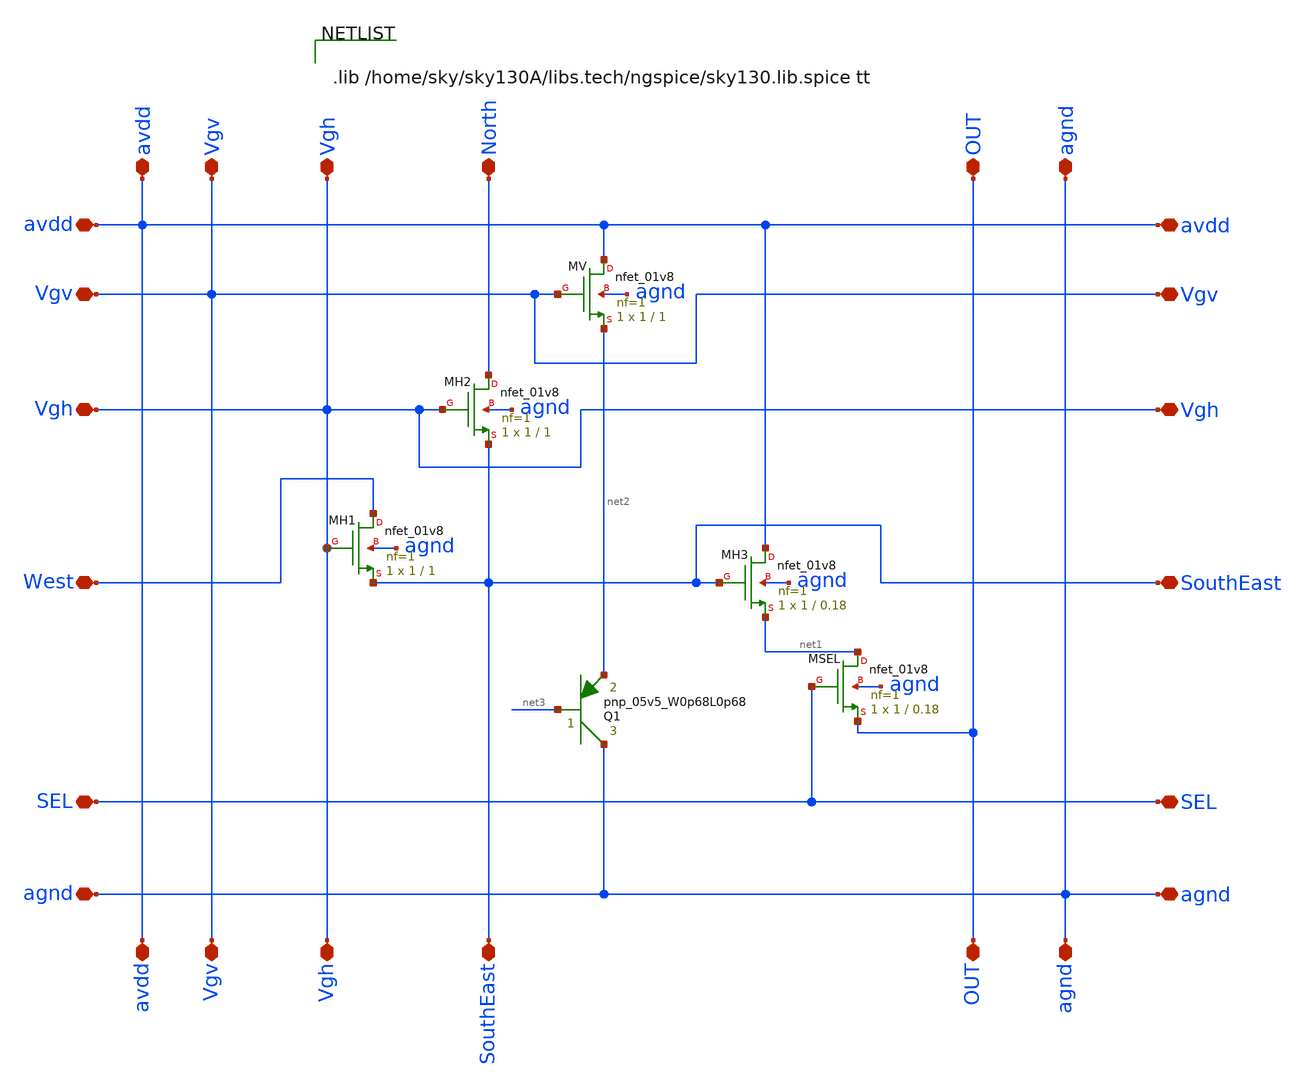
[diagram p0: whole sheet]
** sch_path: xschem/HW4_RAM_readout/pixel.sch
**.subckt pixel North SouthEast West SouthEast avdd avdd avdd avdd Vgv Vgh Vgv Vgv Vgv Vgh Vgh Vgh
*+ SEL SEL OUT OUT agnd agnd agnd agnd
*.iopin North
*.iopin SouthEast
*.iopin West
*.iopin SouthEast
*.iopin avdd
*.iopin avdd
*.iopin avdd
*.iopin avdd
*.iopin Vgv
*.iopin Vgh
*.iopin Vgv
*.iopin Vgv
*.iopin Vgv
*.iopin Vgh
*.iopin Vgh
*.iopin Vgh
*.iopin SEL
*.iopin SEL
*.iopin OUT
*.iopin OUT
*.iopin agnd
*.iopin agnd
*.iopin agnd
*.iopin agnd
XMV avdd Vgv net2 agnd sky130_fd_pr__nfet_01v8 L=1 W=1 nf=1 ad='int((nf+1)/2) * W/nf * 0.29' as='int((nf+2)/2) * W/nf * 0.29'
+ pd='2*int((nf+1)/2) * (W/nf + 0.29)' ps='2*int((nf+2)/2) * (W/nf + 0.29)' nrd='0.29 / W' nrs='0.29 / W'
+ sa=0 sb=0 sd=0 mult=1 m=1
XMH2 North Vgh SouthEast agnd sky130_fd_pr__nfet_01v8 L=1 W=1 nf=1 ad='int((nf+1)/2) * W/nf * 0.29' as='int((nf+2)/2) * W/nf * 0.29'
+ pd='2*int((nf+1)/2) * (W/nf + 0.29)' ps='2*int((nf+2)/2) * (W/nf + 0.29)' nrd='0.29 / W' nrs='0.29 / W'
+ sa=0 sb=0 sd=0 mult=1 m=1
XMH1 West Vgh SouthEast agnd sky130_fd_pr__nfet_01v8 L=1 W=1 nf=1 ad='int((nf+1)/2) * W/nf * 0.29' as='int((nf+2)/2) * W/nf * 0.29'
+ pd='2*int((nf+1)/2) * (W/nf + 0.29)' ps='2*int((nf+2)/2) * (W/nf + 0.29)' nrd='0.29 / W' nrs='0.29 / W'
+ sa=0 sb=0 sd=0 mult=1 m=1
XMH3 avdd SouthEast net1 agnd sky130_fd_pr__nfet_01v8 L=0.18 W=1 nf=1 ad='int((nf+1)/2) * W/nf * 0.29'
+ as='int((nf+2)/2) * W/nf * 0.29' pd='2*int((nf+1)/2) * (W/nf + 0.29)' ps='2*int((nf+2)/2) * (W/nf + 0.29)'
+ nrd='0.29 / W' nrs='0.29 / W' sa=0 sb=0 sd=0 mult=1 m=1
XMSEL net1 SEL OUT agnd sky130_fd_pr__nfet_01v8 L=0.18 W=1 nf=1 ad='int((nf+1)/2) * W/nf * 0.29' as='int((nf+2)/2) * W/nf * 0.29'
+ pd='2*int((nf+1)/2) * (W/nf + 0.29)' ps='2*int((nf+2)/2) * (W/nf + 0.29)' nrd='0.29 / W' nrs='0.29 / W'
+ sa=0 sb=0 sd=0 mult=1 m=1
Q1 agnd net3 net2 pnp_05v5_W0p68L0p68 area=1 m=1
**** begin user architecture code


.lib /home/sky/sky130A/libs.tech/ngspice/sky130.lib.spice tt


**** end user architecture code
**.ends
.end
